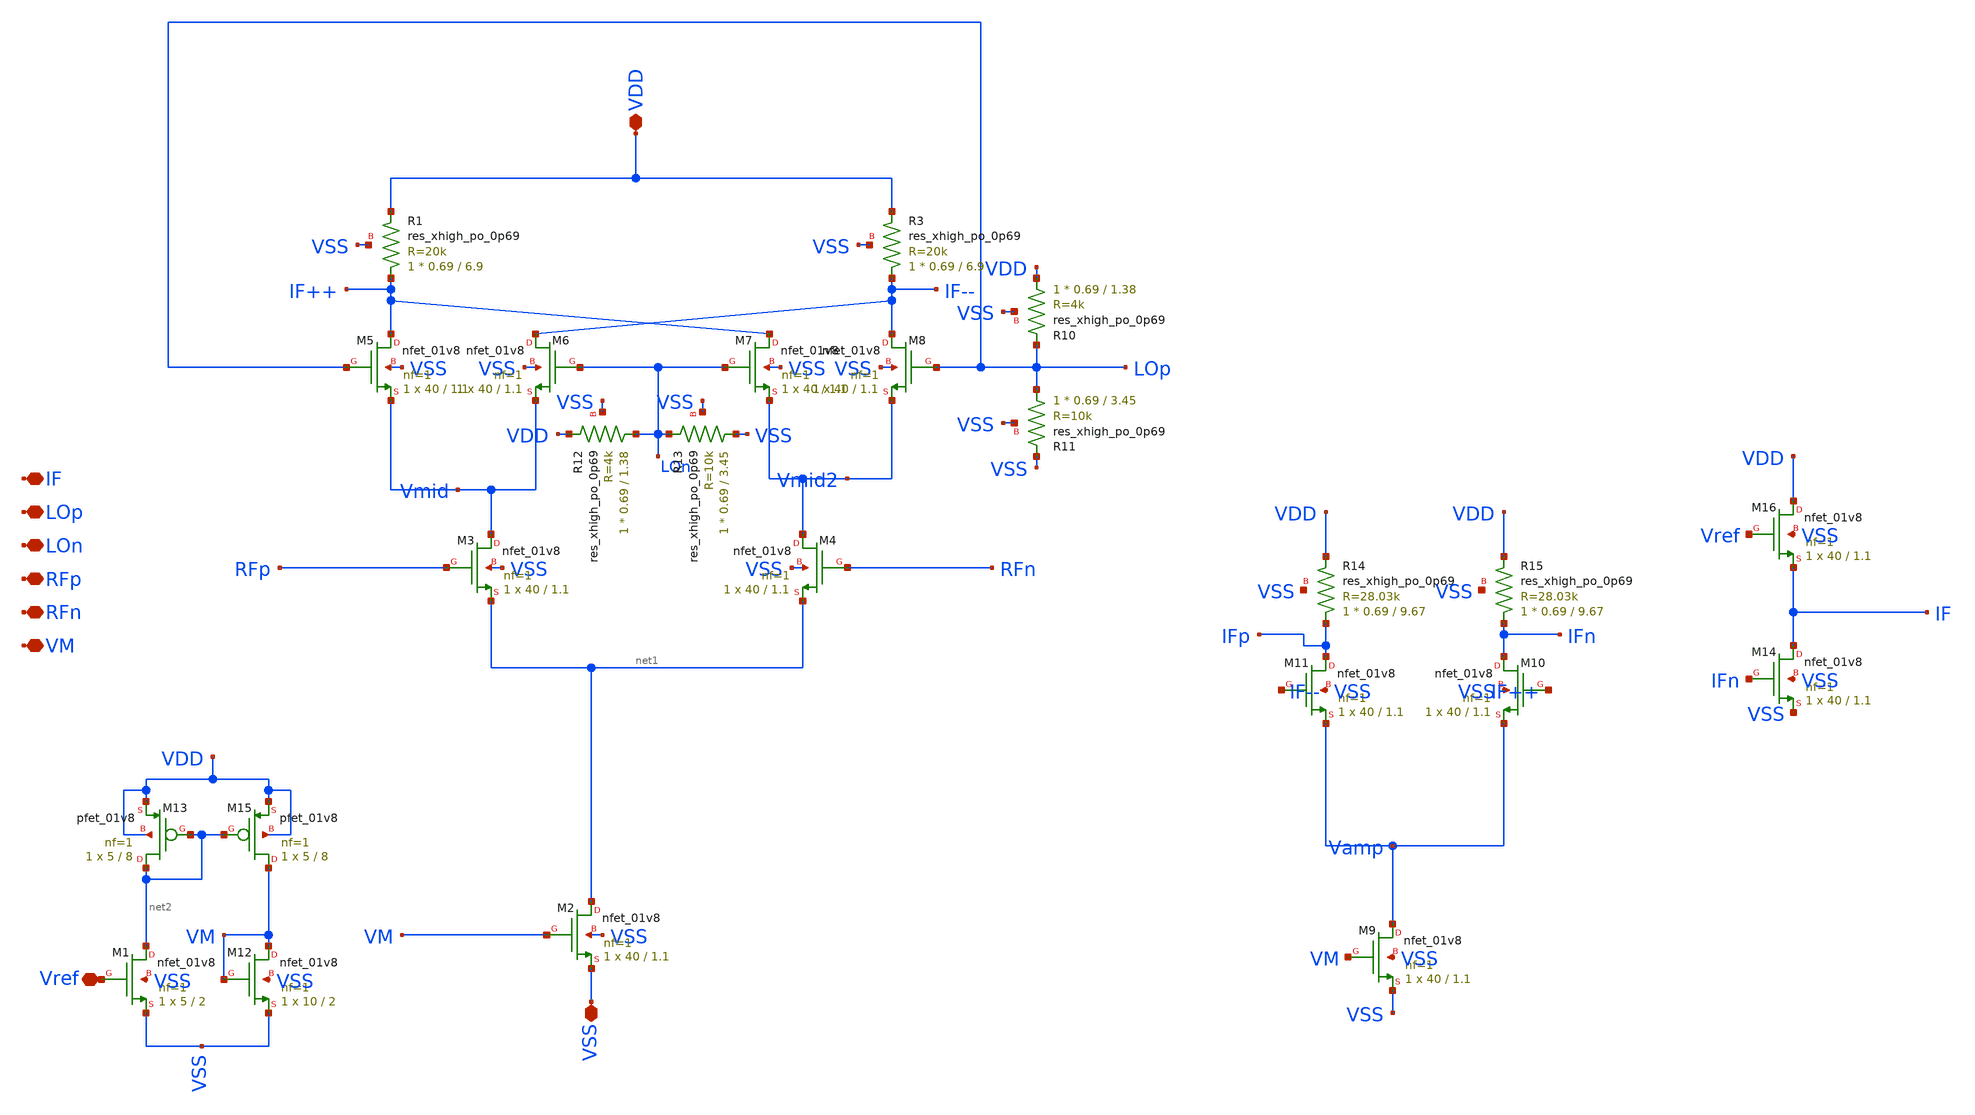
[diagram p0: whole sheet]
** sch_path: Project/xschem/gill_cell.sch
**.subckt gill_cell LOp LOn RFp RFn VDD VSS Vref IF VM
*.iopin LOp
*.iopin LOn
*.iopin RFp
*.iopin RFn
*.iopin VDD
*.iopin VSS
*.iopin Vref
*.iopin IF
*.iopin VM
XR1 IF++ VDD VSS sky130_fd_pr__res_xhigh_po_0p69 L=6.9 mult=1 m=1
XR3 IF-- VDD VSS sky130_fd_pr__res_xhigh_po_0p69 L=6.9 mult=1 m=1
XR10 VDD LOp VSS sky130_fd_pr__res_xhigh_po_0p69 L=1.38 mult=1 m=1
XR11 LOp VSS VSS sky130_fd_pr__res_xhigh_po_0p69 L=3.45 mult=1 m=1
XR12 LOn VDD VSS sky130_fd_pr__res_xhigh_po_0p69 L=1.38 mult=1 m=1
XR13 VSS LOn VSS sky130_fd_pr__res_xhigh_po_0p69 L=3.45 mult=1 m=1
XM2 net1 VM VSS VSS sky130_fd_pr__nfet_01v8 L=1.1 W=40 nf=1 ad='int((nf+1)/2) * W/nf * 0.29' as='int((nf+2)/2) * W/nf * 0.29'
+ pd='2*int((nf+1)/2) * (W/nf + 0.29)' ps='2*int((nf+2)/2) * (W/nf + 0.29)' nrd='0.29 / W' nrs='0.29 / W'
+ sa=0 sb=0 sd=0 mult=1 m=1
XM3 Vmid RFp net1 VSS sky130_fd_pr__nfet_01v8 L=1.1 W=40 nf=1 ad='int((nf+1)/2) * W/nf * 0.29' as='int((nf+2)/2) * W/nf * 0.29'
+ pd='2*int((nf+1)/2) * (W/nf + 0.29)' ps='2*int((nf+2)/2) * (W/nf + 0.29)' nrd='0.29 / W' nrs='0.29 / W'
+ sa=0 sb=0 sd=0 mult=1 m=1
XM5 IF++ LOp Vmid VSS sky130_fd_pr__nfet_01v8 L=1.1 W=40 nf=1 ad='int((nf+1)/2) * W/nf * 0.29' as='int((nf+2)/2) * W/nf * 0.29'
+ pd='2*int((nf+1)/2) * (W/nf + 0.29)' ps='2*int((nf+2)/2) * (W/nf + 0.29)' nrd='0.29 / W' nrs='0.29 / W'
+ sa=0 sb=0 sd=0 mult=1 m=1
XM7 IF++ LOn Vmid2 VSS sky130_fd_pr__nfet_01v8 L=1.1 W=40 nf=1 ad='int((nf+1)/2) * W/nf * 0.29' as='int((nf+2)/2) * W/nf * 0.29'
+ pd='2*int((nf+1)/2) * (W/nf + 0.29)' ps='2*int((nf+2)/2) * (W/nf + 0.29)' nrd='0.29 / W' nrs='0.29 / W'
+ sa=0 sb=0 sd=0 mult=1 m=1
XM4 Vmid2 RFn net1 VSS sky130_fd_pr__nfet_01v8 L=1.1 W=40 nf=1 ad='int((nf+1)/2) * W/nf * 0.29' as='int((nf+2)/2) * W/nf * 0.29'
+ pd='2*int((nf+1)/2) * (W/nf + 0.29)' ps='2*int((nf+2)/2) * (W/nf + 0.29)' nrd='0.29 / W' nrs='0.29 / W'
+ sa=0 sb=0 sd=0 mult=1 m=1
XM8 IF-- LOp Vmid2 VSS sky130_fd_pr__nfet_01v8 L=1.1 W=40 nf=1 ad='int((nf+1)/2) * W/nf * 0.29' as='int((nf+2)/2) * W/nf * 0.29'
+ pd='2*int((nf+1)/2) * (W/nf + 0.29)' ps='2*int((nf+2)/2) * (W/nf + 0.29)' nrd='0.29 / W' nrs='0.29 / W'
+ sa=0 sb=0 sd=0 mult=1 m=1
XM6 IF-- LOn Vmid VSS sky130_fd_pr__nfet_01v8 L=1.1 W=40 nf=1 ad='int((nf+1)/2) * W/nf * 0.29' as='int((nf+2)/2) * W/nf * 0.29'
+ pd='2*int((nf+1)/2) * (W/nf + 0.29)' ps='2*int((nf+2)/2) * (W/nf + 0.29)' nrd='0.29 / W' nrs='0.29 / W'
+ sa=0 sb=0 sd=0 mult=1 m=1
XM9 Vamp VM VSS VSS sky130_fd_pr__nfet_01v8 L=1.1 W=40 nf=1 ad='int((nf+1)/2) * W/nf * 0.29' as='int((nf+2)/2) * W/nf * 0.29'
+ pd='2*int((nf+1)/2) * (W/nf + 0.29)' ps='2*int((nf+2)/2) * (W/nf + 0.29)' nrd='0.29 / W' nrs='0.29 / W'
+ sa=0 sb=0 sd=0 mult=1 m=1
XM10 IFn IF++ Vamp VSS sky130_fd_pr__nfet_01v8 L=1.1 W=40 nf=1 ad='int((nf+1)/2) * W/nf * 0.29' as='int((nf+2)/2) * W/nf * 0.29'
+ pd='2*int((nf+1)/2) * (W/nf + 0.29)' ps='2*int((nf+2)/2) * (W/nf + 0.29)' nrd='0.29 / W' nrs='0.29 / W'
+ sa=0 sb=0 sd=0 mult=1 m=1
XM11 IFp IF-- Vamp VSS sky130_fd_pr__nfet_01v8 L=1.1 W=40 nf=1 ad='int((nf+1)/2) * W/nf * 0.29' as='int((nf+2)/2) * W/nf * 0.29'
+ pd='2*int((nf+1)/2) * (W/nf + 0.29)' ps='2*int((nf+2)/2) * (W/nf + 0.29)' nrd='0.29 / W' nrs='0.29 / W'
+ sa=0 sb=0 sd=0 mult=1 m=1
XR14 IFp VDD VSS sky130_fd_pr__res_xhigh_po_0p69 L=9.67 mult=1 m=1
XR15 IFn VDD VSS sky130_fd_pr__res_xhigh_po_0p69 L=9.67 mult=1 m=1
XM1 net2 Vref VSS VSS sky130_fd_pr__nfet_01v8 L=2 W=5 nf=1 ad='int((nf+1)/2) * W/nf * 0.29' as='int((nf+2)/2) * W/nf * 0.29'
+ pd='2*int((nf+1)/2) * (W/nf + 0.29)' ps='2*int((nf+2)/2) * (W/nf + 0.29)' nrd='0.29 / W' nrs='0.29 / W'
+ sa=0 sb=0 sd=0 mult=1 m=1
XM12 VM VM VSS VSS sky130_fd_pr__nfet_01v8 L=2 W=10 nf=1 ad='int((nf+1)/2) * W/nf * 0.29' as='int((nf+2)/2) * W/nf * 0.29'
+ pd='2*int((nf+1)/2) * (W/nf + 0.29)' ps='2*int((nf+2)/2) * (W/nf + 0.29)' nrd='0.29 / W' nrs='0.29 / W'
+ sa=0 sb=0 sd=0 mult=1 m=1
XM15 VM net2 VDD VDD sky130_fd_pr__pfet_01v8 L=8 W=5 nf=1 ad='int((nf+1)/2) * W/nf * 0.29' as='int((nf+2)/2) * W/nf * 0.29'
+ pd='2*int((nf+1)/2) * (W/nf + 0.29)' ps='2*int((nf+2)/2) * (W/nf + 0.29)' nrd='0.29 / W' nrs='0.29 / W'
+ sa=0 sb=0 sd=0 mult=1 m=1
XM13 net2 net2 VDD VDD sky130_fd_pr__pfet_01v8 L=8 W=5 nf=1 ad='int((nf+1)/2) * W/nf * 0.29' as='int((nf+2)/2) * W/nf * 0.29'
+ pd='2*int((nf+1)/2) * (W/nf + 0.29)' ps='2*int((nf+2)/2) * (W/nf + 0.29)' nrd='0.29 / W' nrs='0.29 / W'
+ sa=0 sb=0 sd=0 mult=1 m=1
XM14 IF IFn VSS VSS sky130_fd_pr__nfet_01v8 L=1.1 W=40 nf=1 ad='int((nf+1)/2) * W/nf * 0.29' as='int((nf+2)/2) * W/nf * 0.29'
+ pd='2*int((nf+1)/2) * (W/nf + 0.29)' ps='2*int((nf+2)/2) * (W/nf + 0.29)' nrd='0.29 / W' nrs='0.29 / W'
+ sa=0 sb=0 sd=0 mult=1 m=1
XM16 VDD Vref IF VSS sky130_fd_pr__nfet_01v8 L=1.1 W=40 nf=1 ad='int((nf+1)/2) * W/nf * 0.29' as='int((nf+2)/2) * W/nf * 0.29'
+ pd='2*int((nf+1)/2) * (W/nf + 0.29)' ps='2*int((nf+2)/2) * (W/nf + 0.29)' nrd='0.29 / W' nrs='0.29 / W'
+ sa=0 sb=0 sd=0 mult=1 m=1
**.ends
.end
